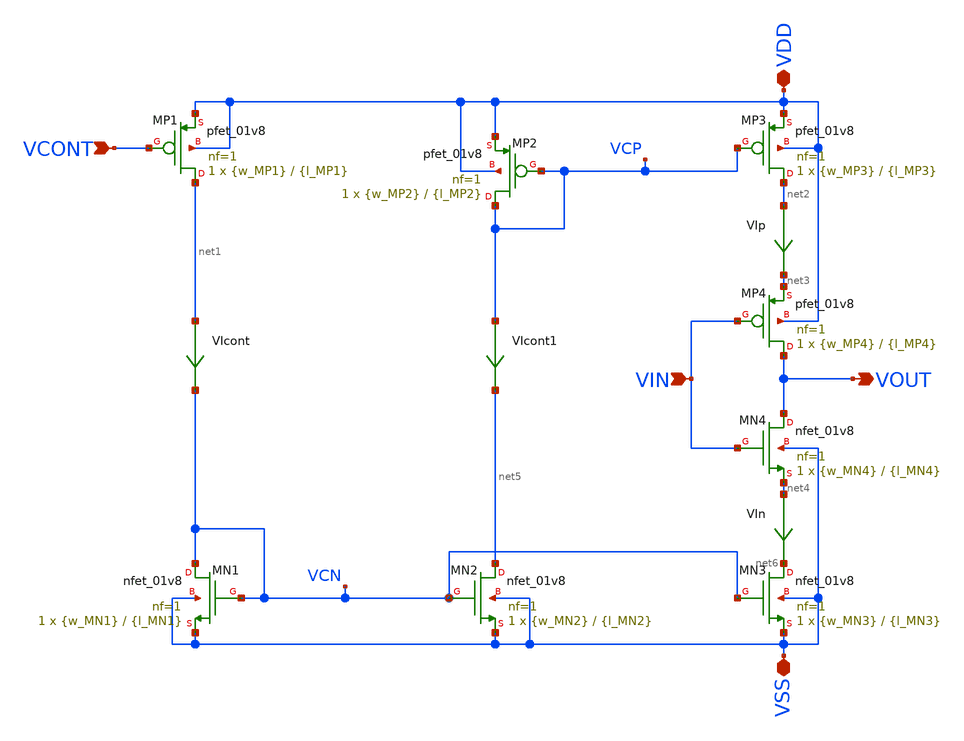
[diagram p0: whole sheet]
** sch_path: xschem/VCO/stage_V0.sch
**.subckt stage_V0 VIN VOUT VDD VSS VCONT
*.ipin VIN
*.opin VOUT
*.iopin VDD
*.iopin VSS
*.ipin VCONT
XMP1 net1 VCONT VDD VDD sky130_fd_pr__pfet_01v8 L={l_MP1} W={w_MP1} nf=1 ad='int((nf+1)/2) * W/nf * 0.29'
+ as='int((nf+2)/2) * W/nf * 0.29' pd='2*int((nf+1)/2) * (W/nf + 0.29)' ps='2*int((nf+2)/2) * (W/nf + 0.29)'
+ nrd='0.29 / W' nrs='0.29 / W' sa=0 sb=0 sd=0 mult=1 m=1
XMP2 VCP VCP VDD VDD sky130_fd_pr__pfet_01v8 L={l_MP2} W={w_MP2} nf=1 ad='int((nf+1)/2) * W/nf * 0.29'
+ as='int((nf+2)/2) * W/nf * 0.29' pd='2*int((nf+1)/2) * (W/nf + 0.29)' ps='2*int((nf+2)/2) * (W/nf + 0.29)'
+ nrd='0.29 / W' nrs='0.29 / W' sa=0 sb=0 sd=0 mult=1 m=1
XMP3 net2 VCP VDD VDD sky130_fd_pr__pfet_01v8 L={l_MP3} W={w_MP3} nf=1 ad='int((nf+1)/2) * W/nf * 0.29'
+ as='int((nf+2)/2) * W/nf * 0.29' pd='2*int((nf+1)/2) * (W/nf + 0.29)' ps='2*int((nf+2)/2) * (W/nf + 0.29)'
+ nrd='0.29 / W' nrs='0.29 / W' sa=0 sb=0 sd=0 mult=1 m=1
XMP4 VOUT VIN net3 VDD sky130_fd_pr__pfet_01v8 L={l_MP4} W={w_MP4} nf=1 ad='int((nf+1)/2) * W/nf * 0.29'
+ as='int((nf+2)/2) * W/nf * 0.29' pd='2*int((nf+1)/2) * (W/nf + 0.29)' ps='2*int((nf+2)/2) * (W/nf + 0.29)'
+ nrd='0.29 / W' nrs='0.29 / W' sa=0 sb=0 sd=0 mult=1 m=1
XMN1 VCN VCN VSS VSS sky130_fd_pr__nfet_01v8 L={l_MN1} W={w_MN1} nf=1 ad='int((nf+1)/2) * W/nf * 0.29'
+ as='int((nf+2)/2) * W/nf * 0.29' pd='2*int((nf+1)/2) * (W/nf + 0.29)' ps='2*int((nf+2)/2) * (W/nf + 0.29)'
+ nrd='0.29 / W' nrs='0.29 / W' sa=0 sb=0 sd=0 mult=1 m=1
XMN2 net5 VCN VSS VSS sky130_fd_pr__nfet_01v8 L={l_MN2} W={w_MN2} nf=1 ad='int((nf+1)/2) * W/nf * 0.29'
+ as='int((nf+2)/2) * W/nf * 0.29' pd='2*int((nf+1)/2) * (W/nf + 0.29)' ps='2*int((nf+2)/2) * (W/nf + 0.29)'
+ nrd='0.29 / W' nrs='0.29 / W' sa=0 sb=0 sd=0 mult=1 m=1
XMN3 net6 VCN VSS VSS sky130_fd_pr__nfet_01v8 L={l_MN3} W={w_MN3} nf=1 ad='int((nf+1)/2) * W/nf * 0.29'
+ as='int((nf+2)/2) * W/nf * 0.29' pd='2*int((nf+1)/2) * (W/nf + 0.29)' ps='2*int((nf+2)/2) * (W/nf + 0.29)'
+ nrd='0.29 / W' nrs='0.29 / W' sa=0 sb=0 sd=0 mult=1 m=1
XMN4 VOUT VIN net4 VSS sky130_fd_pr__nfet_01v8 L={l_MN4} W={w_MN4} nf=1 ad='int((nf+1)/2) * W/nf * 0.29'
+ as='int((nf+2)/2) * W/nf * 0.29' pd='2*int((nf+1)/2) * (W/nf + 0.29)' ps='2*int((nf+2)/2) * (W/nf + 0.29)'
+ nrd='0.29 / W' nrs='0.29 / W' sa=0 sb=0 sd=0 mult=1 m=1
VIcont net1 VCN 0
.save i(vicont)
VIp net2 net3 0
.save i(vip)
VIn net4 net6 0
.save i(vin)
VIcont1 VCP net5 0
.save i(vicont1)
**.ends
.end
